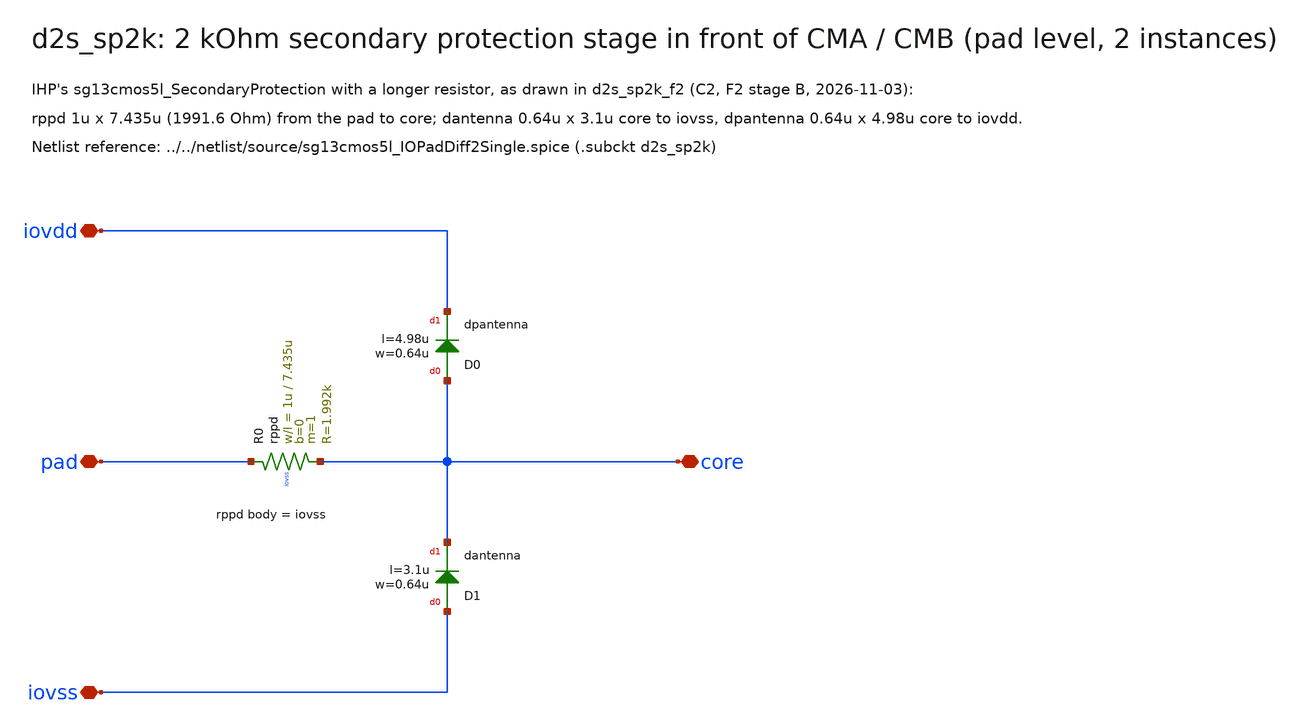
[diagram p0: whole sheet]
** sch_path: macros/sg13cmos5l_IOPadDiff2Single/schematic/xschem/d2s_sp2k.sch
**.subckt d2s_sp2k core iovdd iovss pad
*.iopin core
*.iopin iovdd
*.iopin iovss
*.iopin pad
XR0 pad core iovss rppd w=1u l=7.435u m=1 b=0 mm_ok=1
XD0 core iovdd dpantenna l=4.98u w=0.64u
XD1 iovss core dantenna l=3.1u w=0.64u
**.ends
.end
